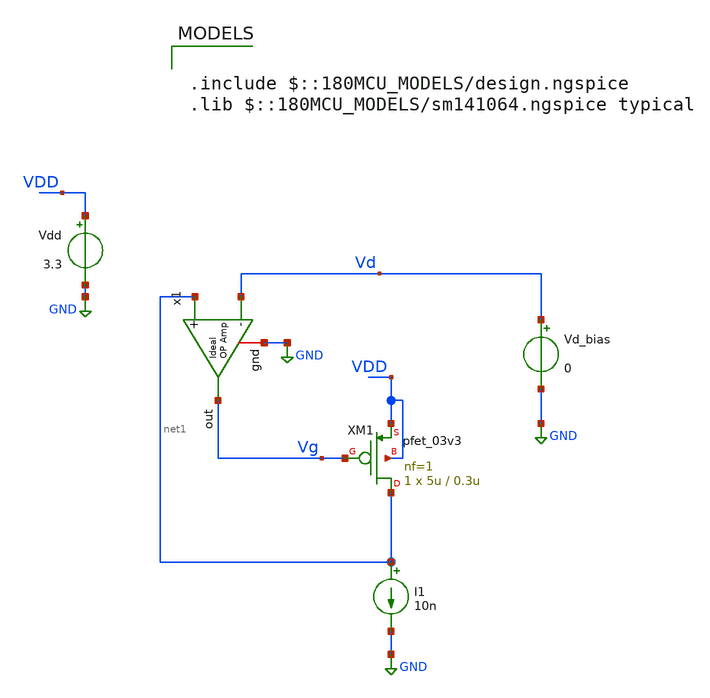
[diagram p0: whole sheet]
** sch_path: ihp_tutorials/Extraction/pmos_sigma_ext.sch
**.subckt pmos_sigma_ext
x1 Vg net1 Vd GND ampOp_ideal
I1 net1 GND 10n
Vd_bias Vd GND 0
Vdd VDD GND 3.3
XM1 net1 Vg VDD VDD pfet_03v3 L=0.3u W=5u nf=1 ad='int((nf+1)/2) * W/nf * 0.18u' as='int((nf+2)/2) * W/nf * 0.18u'
+ pd='2*int((nf+1)/2) * (W/nf + 0.18u)' ps='2*int((nf+2)/2) * (W/nf + 0.18u)' nrd='0.18u / W' nrs='0.18u / W'
+ sa=0 sb=0 sd=0 m=1
**** begin user architecture code

.include $::180MCU_MODELS/design.ngspice
.lib $::180MCU_MODELS/sm141064.ngspice typical




.control
save all

dc Vd_bias  0 -4 -25.9m

let vd_interp = -3.3/3
let sigma = -deriv(V(vg))/deriv(V(vd))
save sigma

echo
echo
echo


echo Sigma @ VD=$&vd_interp:
meas dc sigma_value FIND sigma WHEN V(vd)=vd_interp

echo
echo
echo
write pmos_sigma_ext.raw

.endc




**** end user architecture code
**.ends

* expanding   symbol:  /home/gmaranhao/Desktop/gf180_work/auxLib/ampOp_ideal.sym # of pins=4
** sym_path: gf_tutorials/auxLib/ampOp_ideal.sym
** sch_path: gf_tutorials/auxLib/ampOp_ideal.sch
.subckt ampOp_ideal out + - gnd
*.ipin +
*.ipin -
*.opin out
*.iopin gnd
E1 out gnd + - 10000000
.ends

.GLOBAL GND
.end
